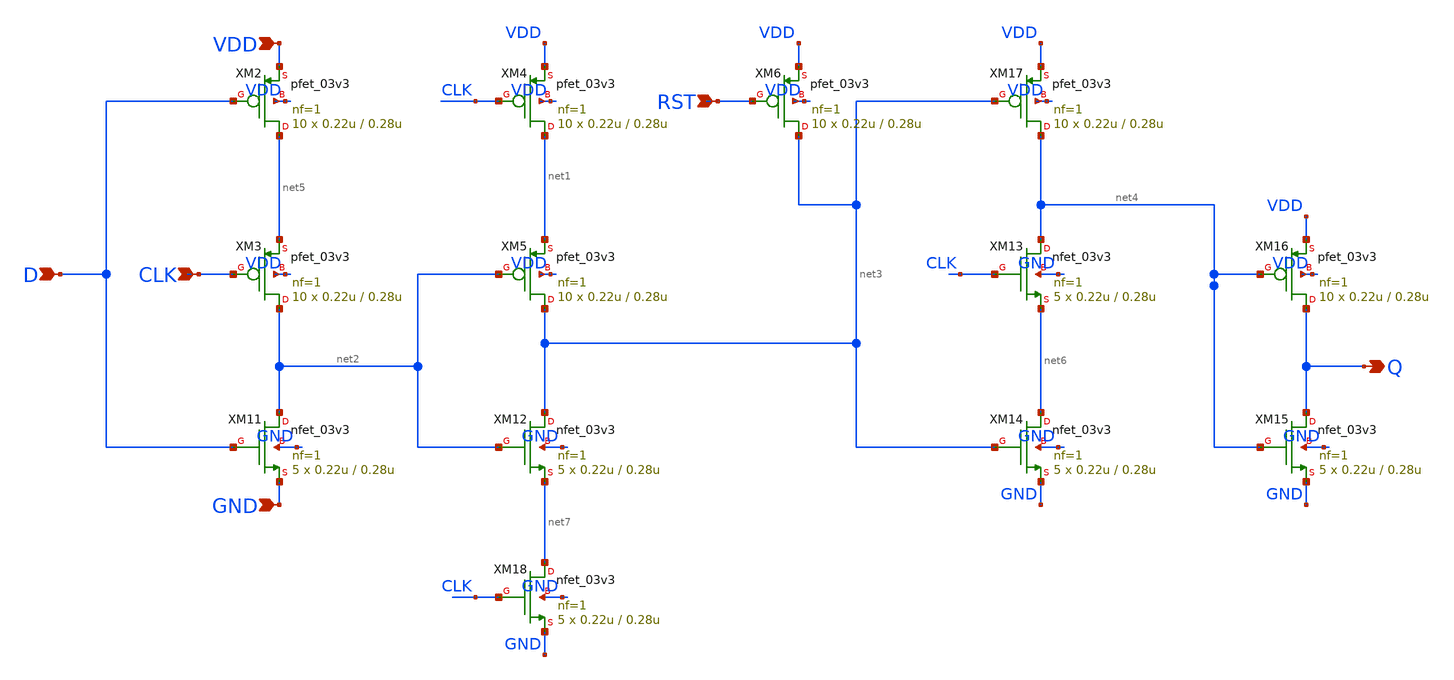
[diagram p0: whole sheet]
** sch_path: blocks/adc/encoder/sym/dff_encoder.sch
**.subckt dff_encoder Q D CLK RST VDD GND
*.opin Q
*.ipin D
*.ipin CLK
*.ipin RST
*.ipin VDD
*.ipin GND
XM2 net5 D VDD VDD pfet_03v3 L=0.28u W=0.22u nf=1 ad='int((nf+1)/2) * W/nf * 0.18u' as='int((nf+2)/2) * W/nf * 0.18u'
+ pd='2*int((nf+1)/2) * (W/nf + 0.18u)' ps='2*int((nf+2)/2) * (W/nf + 0.18u)' nrd='0.18u / W' nrs='0.18u / W'
+ sa=0 sb=0 sd=0 m=10
XM3 net2 CLK net5 VDD pfet_03v3 L=0.28u W=0.22u nf=1 ad='int((nf+1)/2) * W/nf * 0.18u' as='int((nf+2)/2) * W/nf * 0.18u'
+ pd='2*int((nf+1)/2) * (W/nf + 0.18u)' ps='2*int((nf+2)/2) * (W/nf + 0.18u)' nrd='0.18u / W' nrs='0.18u / W'
+ sa=0 sb=0 sd=0 m=10
XM4 net1 CLK VDD VDD pfet_03v3 L=0.28u W=0.22u nf=1 ad='int((nf+1)/2) * W/nf * 0.18u' as='int((nf+2)/2) * W/nf * 0.18u'
+ pd='2*int((nf+1)/2) * (W/nf + 0.18u)' ps='2*int((nf+2)/2) * (W/nf + 0.18u)' nrd='0.18u / W' nrs='0.18u / W'
+ sa=0 sb=0 sd=0 m=10
XM5 net3 net2 net1 VDD pfet_03v3 L=0.28u W=0.22u nf=1 ad='int((nf+1)/2) * W/nf * 0.18u' as='int((nf+2)/2) * W/nf * 0.18u'
+ pd='2*int((nf+1)/2) * (W/nf + 0.18u)' ps='2*int((nf+2)/2) * (W/nf + 0.18u)' nrd='0.18u / W' nrs='0.18u / W'
+ sa=0 sb=0 sd=0 m=10
XM6 net3 RST VDD VDD pfet_03v3 L=0.28u W=0.22u nf=1 ad='int((nf+1)/2) * W/nf * 0.18u' as='int((nf+2)/2) * W/nf * 0.18u'
+ pd='2*int((nf+1)/2) * (W/nf + 0.18u)' ps='2*int((nf+2)/2) * (W/nf + 0.18u)' nrd='0.18u / W' nrs='0.18u / W'
+ sa=0 sb=0 sd=0 m=10
XM11 net2 D GND GND nfet_03v3 L=0.28u W=0.22u nf=1 ad='int((nf+1)/2) * W/nf * 0.18u' as='int((nf+2)/2) * W/nf * 0.18u'
+ pd='2*int((nf+1)/2) * (W/nf + 0.18u)' ps='2*int((nf+2)/2) * (W/nf + 0.18u)' nrd='0.18u / W' nrs='0.18u / W'
+ sa=0 sb=0 sd=0 m=5
XM12 net3 net2 net7 GND nfet_03v3 L=0.28u W=0.22u nf=1 ad='int((nf+1)/2) * W/nf * 0.18u' as='int((nf+2)/2) * W/nf * 0.18u'
+ pd='2*int((nf+1)/2) * (W/nf + 0.18u)' ps='2*int((nf+2)/2) * (W/nf + 0.18u)' nrd='0.18u / W' nrs='0.18u / W'
+ sa=0 sb=0 sd=0 m=5
XM13 net4 CLK net6 GND nfet_03v3 L=0.28u W=0.22u nf=1 ad='int((nf+1)/2) * W/nf * 0.18u' as='int((nf+2)/2) * W/nf * 0.18u'
+ pd='2*int((nf+1)/2) * (W/nf + 0.18u)' ps='2*int((nf+2)/2) * (W/nf + 0.18u)' nrd='0.18u / W' nrs='0.18u / W'
+ sa=0 sb=0 sd=0 m=5
XM14 net6 net3 GND GND nfet_03v3 L=0.28u W=0.22u nf=1 ad='int((nf+1)/2) * W/nf * 0.18u' as='int((nf+2)/2) * W/nf * 0.18u'
+ pd='2*int((nf+1)/2) * (W/nf + 0.18u)' ps='2*int((nf+2)/2) * (W/nf + 0.18u)' nrd='0.18u / W' nrs='0.18u / W'
+ sa=0 sb=0 sd=0 m=5
XM15 Q net4 GND GND nfet_03v3 L=0.28u W=0.22u nf=1 ad='int((nf+1)/2) * W/nf * 0.18u' as='int((nf+2)/2) * W/nf * 0.18u'
+ pd='2*int((nf+1)/2) * (W/nf + 0.18u)' ps='2*int((nf+2)/2) * (W/nf + 0.18u)' nrd='0.18u / W' nrs='0.18u / W'
+ sa=0 sb=0 sd=0 m=5
XM16 Q net4 VDD VDD pfet_03v3 L=0.28u W=0.22u nf=1 ad='int((nf+1)/2) * W/nf * 0.18u' as='int((nf+2)/2) * W/nf * 0.18u'
+ pd='2*int((nf+1)/2) * (W/nf + 0.18u)' ps='2*int((nf+2)/2) * (W/nf + 0.18u)' nrd='0.18u / W' nrs='0.18u / W'
+ sa=0 sb=0 sd=0 m=10
XM17 net4 net3 VDD VDD pfet_03v3 L=0.28u W=0.22u nf=1 ad='int((nf+1)/2) * W/nf * 0.18u' as='int((nf+2)/2) * W/nf * 0.18u'
+ pd='2*int((nf+1)/2) * (W/nf + 0.18u)' ps='2*int((nf+2)/2) * (W/nf + 0.18u)' nrd='0.18u / W' nrs='0.18u / W'
+ sa=0 sb=0 sd=0 m=10
XM18 net7 CLK GND GND nfet_03v3 L=0.28u W=0.22u nf=1 ad='int((nf+1)/2) * W/nf * 0.18u' as='int((nf+2)/2) * W/nf * 0.18u'
+ pd='2*int((nf+1)/2) * (W/nf + 0.18u)' ps='2*int((nf+2)/2) * (W/nf + 0.18u)' nrd='0.18u / W' nrs='0.18u / W'
+ sa=0 sb=0 sd=0 m=5
**.ends
.end
